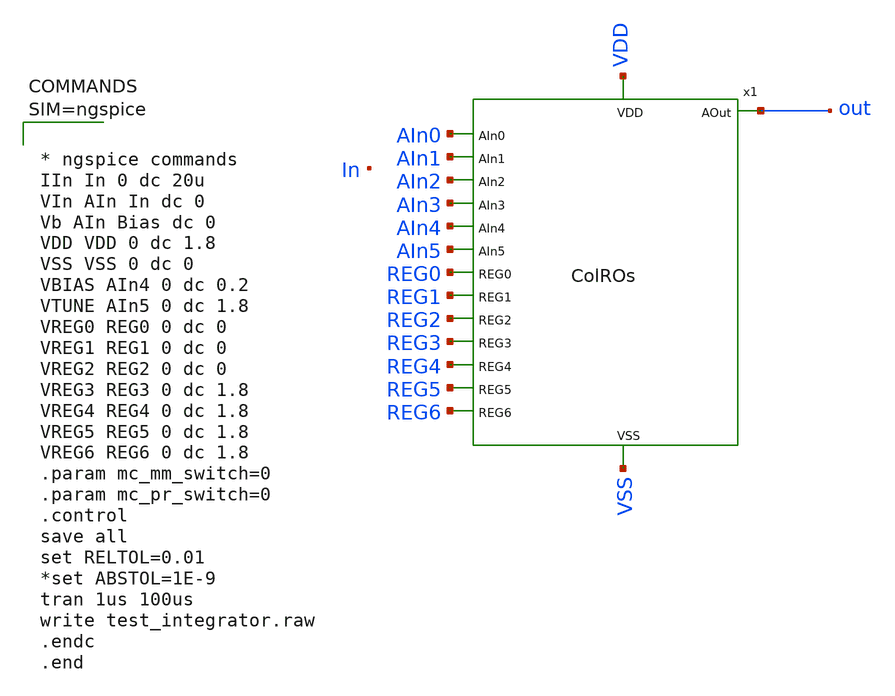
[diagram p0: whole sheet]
** sch_path: xschem/test_ColROs.sch
**.subckt test_ColROs
x1 VDD VSS AIn0 out AIn1 AIn2 AIn3 AIn4 AIn5 REG0 REG1 REG2 REG3 REG4 REG5 REG6 ColROs
**** begin user architecture code

** opencircuitdesign pdks install
.lib $::SKYWATER_MODELS/sky130.lib.spice tt





* ngspice commands
IIn In 0 dc 20u
VIn AIn In dc 0
Vb AIn Bias dc 0
VDD VDD 0 dc 1.8
VSS VSS 0 dc 0
VBIAS AIn4 0 dc 0.2
VTUNE AIn5 0 dc 1.8
VREG0 REG0 0 dc 0
VREG1 REG1 0 dc 0
VREG2 REG2 0 dc 0
VREG3 REG3 0 dc 1.8
VREG4 REG4 0 dc 1.8
VREG5 REG5 0 dc 1.8
VREG6 REG6 0 dc 1.8
.param mc_mm_switch=0
.param mc_pr_switch=0
.control
save all
set RELTOL=0.01
*set ABSTOL=1E-9
tran 1us 100us
write test_integrator.raw
.endc
.end


**** end user architecture code
**.ends
.end
